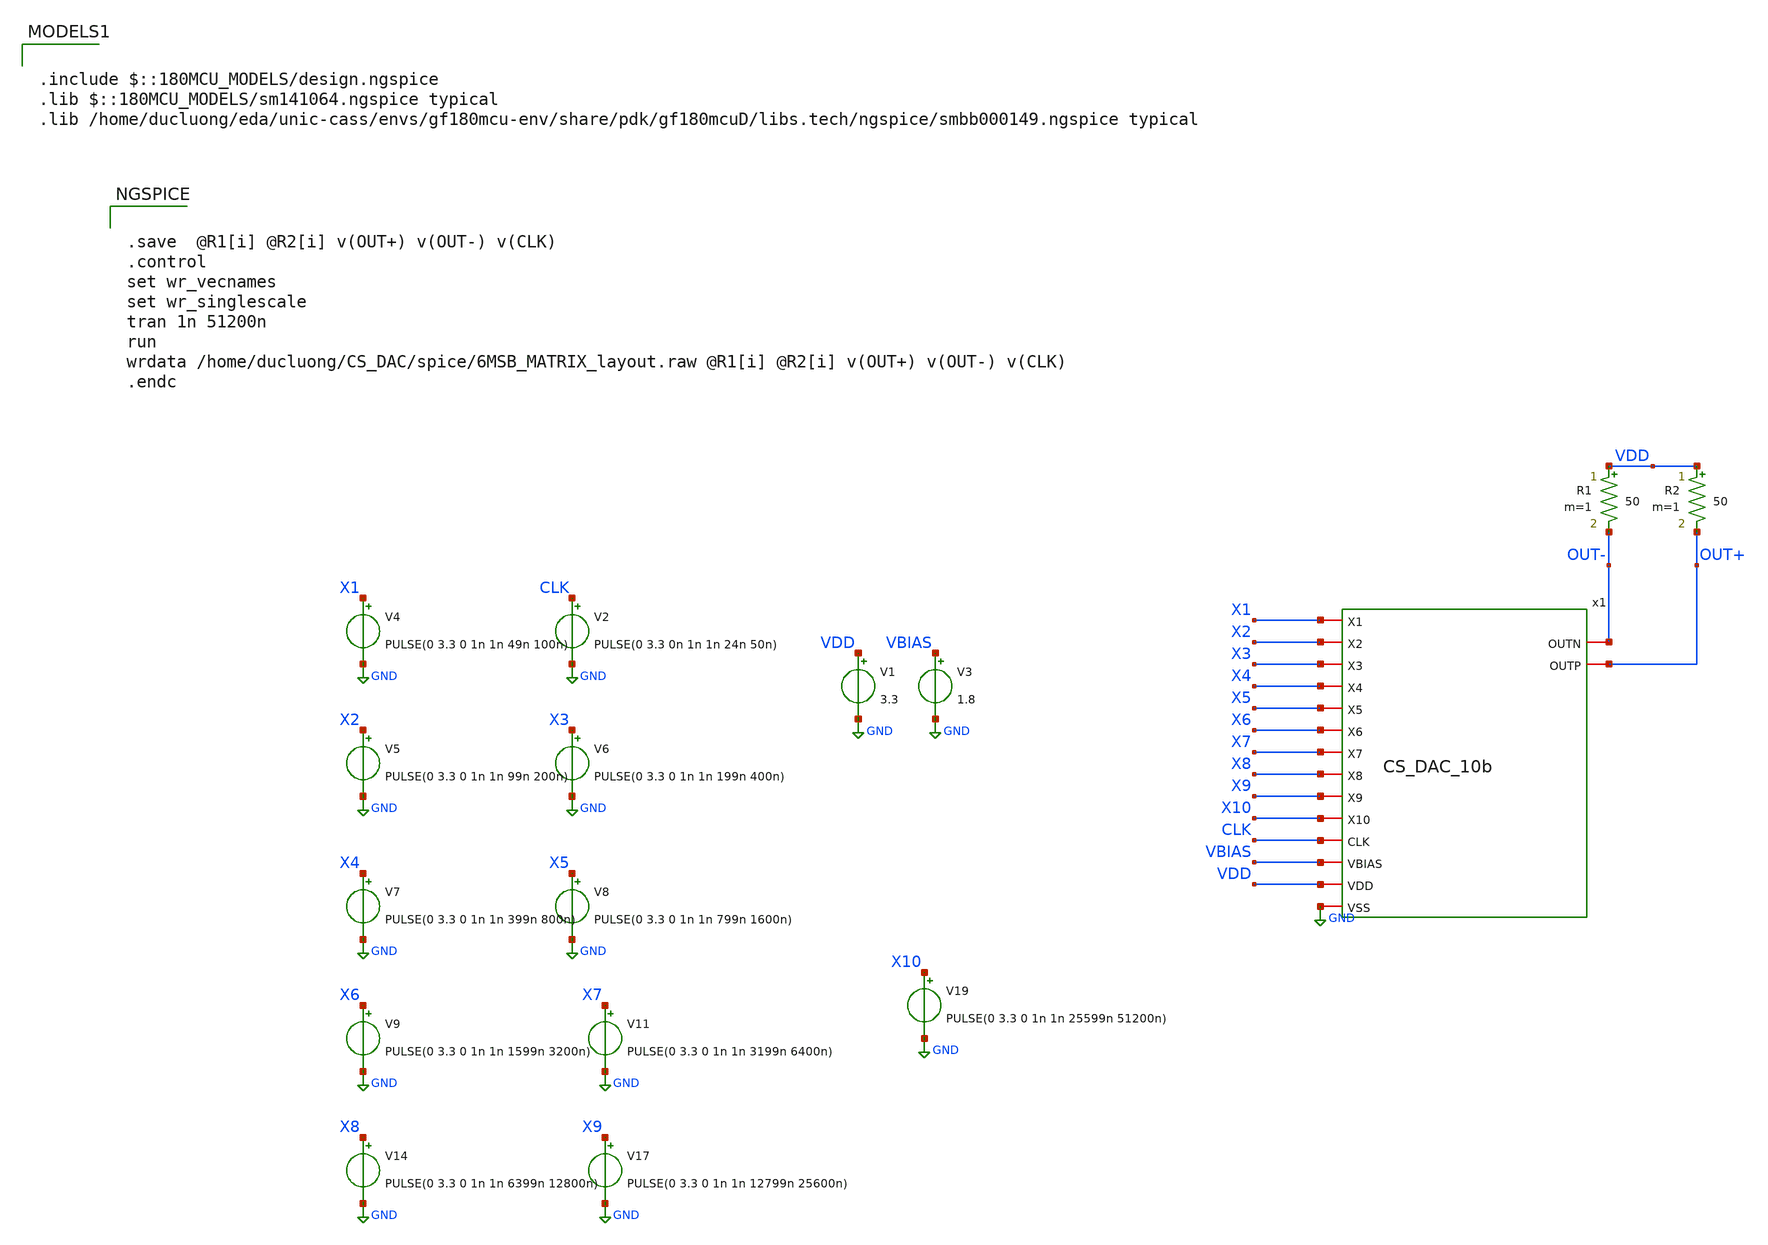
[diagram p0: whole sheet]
** sch_path: xschem/CS_DAC_10b_tb.sch
**.subckt CS_DAC_10b_tb
V1 VDD GND 3.3
V3 VBIAS GND 1.8
V2 CLK GND PULSE(0 3.3 0n 1n 1n 24n 50n)
V4 X1 GND PULSE(0 3.3 0 1n 1n 49n 100n)
V5 X2 GND PULSE(0 3.3 0 1n 1n 99n 200n)
V6 X3 GND PULSE(0 3.3 0 1n 1n 199n 400n)
V7 X4 GND PULSE(0 3.3 0 1n 1n 399n 800n)
V8 X5 GND PULSE(0 3.3 0 1n 1n 799n 1600n)
V9 X6 GND PULSE(0 3.3 0 1n 1n 1599n 3200n)
V11 X7 GND PULSE(0 3.3 0 1n 1n 3199n 6400n)
V14 X8 GND PULSE(0 3.3 0 1n 1n 6399n 12800n)
V17 X9 GND PULSE(0 3.3 0 1n 1n 12799n 25600n)
V19 X10 GND PULSE(0 3.3 0 1n 1n 25599n 51200n)
x1 X1 X2 X3 X4 X5 X6 X7 X8 X9 X10 CLK OUT+ OUT- VBIAS VDD GND CS_DAC_10b
R1 VDD OUT- 50 m=1
R2 VDD OUT+ 50 m=1
**** begin user architecture code

.include $::180MCU_MODELS/design.ngspice
.lib $::180MCU_MODELS/sm141064.ngspice typical
.lib /home/ducluong/eda/unic-cass/envs/gf180mcu-env/share/pdk/gf180mcuD/libs.tech/ngspice/smbb000149.ngspice typical


.save  @R1[i] @R2[i] v(OUT+) v(OUT-) v(CLK)
.control
set wr_vecnames
set wr_singlescale
tran 1n 51200n
run
wrdata /home/ducluong/CS_DAC/spice/6MSB_MATRIX_layout.raw @R1[i] @R2[i] v(OUT+) v(OUT-) v(CLK)
.endc


 .inc /home/ducluong/CS_DAC/Magic_gf180mcuD/CS_DAC_10b.spice
**** end user architecture code
**.ends
.GLOBAL GND
.end
